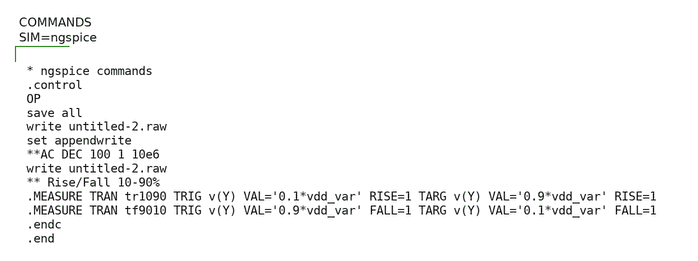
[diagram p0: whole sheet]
** sch_path: xschem/untitled-2.sch
**.subckt untitled-2
**** begin user architecture code



* ngspice commands
.control
OP
save all
write untitled-2.raw
set appendwrite
**AC DEC 100 1 10e6
write untitled-2.raw
** Rise/Fall 10-90%
.MEASURE TRAN tr1090 TRIG v(Y) VAL='0.1*vdd_var' RISE=1 TARG v(Y) VAL='0.9*vdd_var' RISE=1
.MEASURE TRAN tf9010 TRIG v(Y) VAL='0.9*vdd_var' FALL=1 TARG v(Y) VAL='0.1*vdd_var' FALL=1
.endc
.end



**** end user architecture code
**.ends
.end
